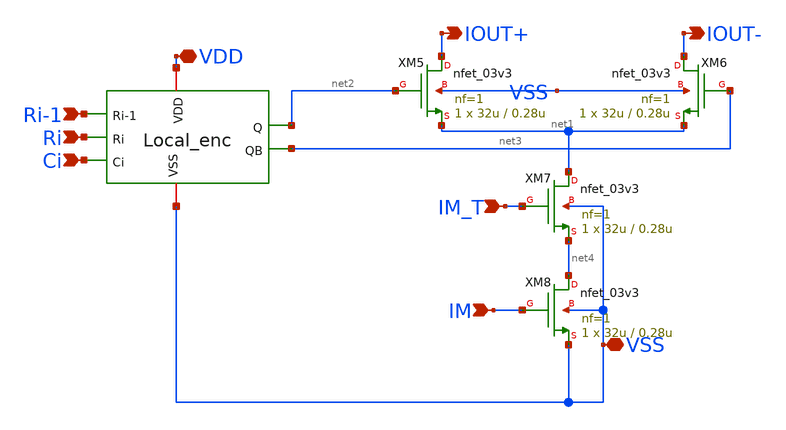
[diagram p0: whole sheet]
** sch_path: DAC_PAKISTAN_01/Pakistan1_Xschem/MSB_Unit_Cell_V2.sch
**.subckt MSB_Unit_Cell_V2 VDD VSS Ri-1 Ri Ci IM_T IM IOUT+ IOUT-
*.iopin VDD
*.iopin VSS
*.ipin Ri-1
*.ipin Ri
*.ipin Ci
*.ipin IM_T
*.ipin IM
*.opin IOUT+
*.opin IOUT-
x1 VDD VSS Ri-1 Ri Ci net2 net3 Local_Enc
XM5 IOUT+ net2 net1 VSS nfet_03v3 L=0.28u W=32u nf=1 ad='int((nf+1)/2) * W/nf * 0.18u' as='int((nf+2)/2) * W/nf * 0.18u'
+ pd='2*int((nf+1)/2) * (W/nf + 0.18u)' ps='2*int((nf+2)/2) * (W/nf + 0.18u)' nrd='0.18u / W' nrs='0.18u / W'
+ sa=0 sb=0 sd=0 m=1
XM6 IOUT- net3 net1 VSS nfet_03v3 L=0.28u W=32u nf=1 ad='int((nf+1)/2) * W/nf * 0.18u' as='int((nf+2)/2) * W/nf * 0.18u'
+ pd='2*int((nf+1)/2) * (W/nf + 0.18u)' ps='2*int((nf+2)/2) * (W/nf + 0.18u)' nrd='0.18u / W' nrs='0.18u / W'
+ sa=0 sb=0 sd=0 m=1
XM7 net1 IM_T net4 VSS nfet_03v3 L=0.28u W=32u nf=1 ad='int((nf+1)/2) * W/nf * 0.18u' as='int((nf+2)/2) * W/nf * 0.18u'
+ pd='2*int((nf+1)/2) * (W/nf + 0.18u)' ps='2*int((nf+2)/2) * (W/nf + 0.18u)' nrd='0.18u / W' nrs='0.18u / W'
+ sa=0 sb=0 sd=0 m=1
XM8 net4 IM VSS VSS nfet_03v3 L=0.28u W=32u nf=1 ad='int((nf+1)/2) * W/nf * 0.18u' as='int((nf+2)/2) * W/nf * 0.18u'
+ pd='2*int((nf+1)/2) * (W/nf + 0.18u)' ps='2*int((nf+2)/2) * (W/nf + 0.18u)' nrd='0.18u / W' nrs='0.18u / W'
+ sa=0 sb=0 sd=0 m=1
**.ends
.end
